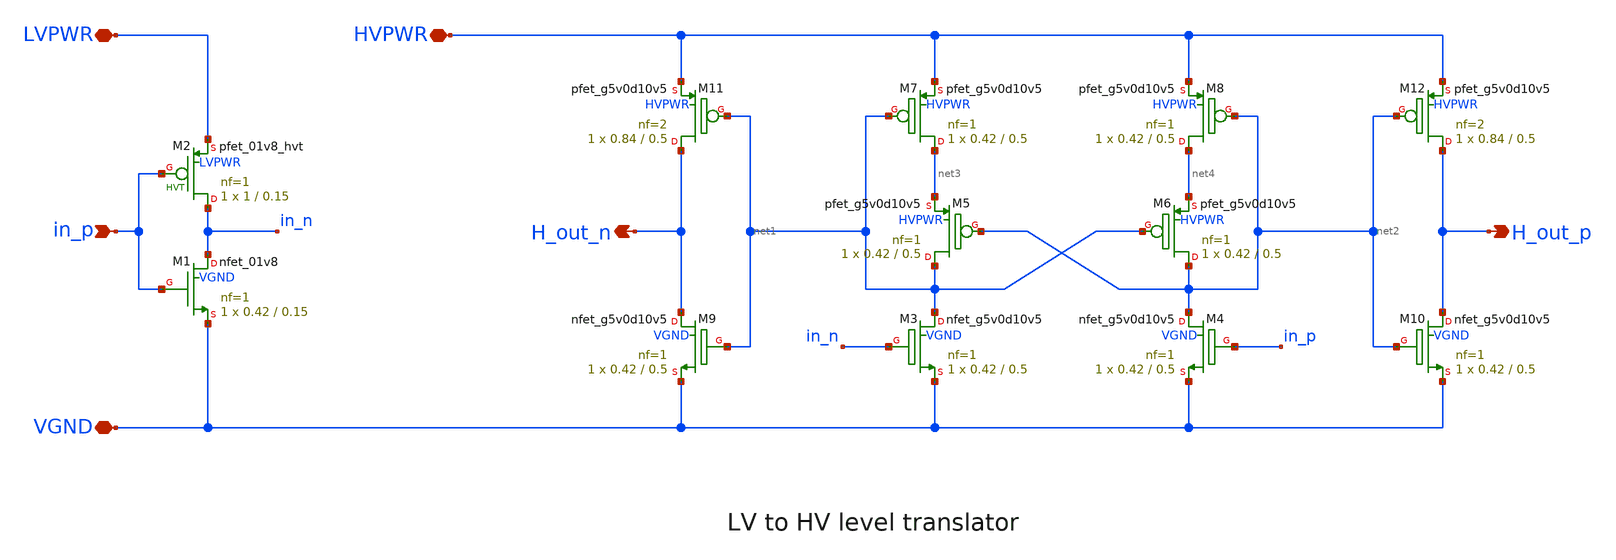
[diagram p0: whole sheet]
** sch_path: tt_um_analog_factory_test/xschem/lv2hv.sch
**.subckt lv2hv in_p VGND LVPWR HVPWR H_out_p H_out_n
*.ipin in_p
*.iopin VGND
*.iopin LVPWR
*.iopin HVPWR
*.opin H_out_p
*.opin H_out_n
XM12 H_out_p net2 HVPWR HVPWR sky130_fd_pr__pfet_g5v0d10v5 L=0.5 W=0.84 nf=2 ad='int((nf+1)/2) * W/nf * 0.29'
+ as='int((nf+2)/2) * W/nf * 0.29' pd='2*int((nf+1)/2) * (W/nf + 0.29)' ps='2*int((nf+2)/2) * (W/nf + 0.29)'
+ nrd='0.29 / W' nrs='0.29 / W' sa=0 sb=0 sd=0 mult=1 m=1
XM10 H_out_p net2 VGND VGND sky130_fd_pr__nfet_g5v0d10v5 L=0.5 W=0.42 nf=1 ad='int((nf+1)/2) * W/nf * 0.29'
+ as='int((nf+2)/2) * W/nf * 0.29' pd='2*int((nf+1)/2) * (W/nf + 0.29)' ps='2*int((nf+2)/2) * (W/nf + 0.29)'
+ nrd='0.29 / W' nrs='0.29 / W' sa=0 sb=0 sd=0 mult=1 m=1
XM11 H_out_n net1 HVPWR HVPWR sky130_fd_pr__pfet_g5v0d10v5 L=0.5 W=0.84 nf=2 ad='int((nf+1)/2) * W/nf * 0.29'
+ as='int((nf+2)/2) * W/nf * 0.29' pd='2*int((nf+1)/2) * (W/nf + 0.29)' ps='2*int((nf+2)/2) * (W/nf + 0.29)'
+ nrd='0.29 / W' nrs='0.29 / W' sa=0 sb=0 sd=0 mult=1 m=1
XM9 H_out_n net1 VGND VGND sky130_fd_pr__nfet_g5v0d10v5 L=0.5 W=0.42 nf=1 ad='int((nf+1)/2) * W/nf * 0.29'
+ as='int((nf+2)/2) * W/nf * 0.29' pd='2*int((nf+1)/2) * (W/nf + 0.29)' ps='2*int((nf+2)/2) * (W/nf + 0.29)'
+ nrd='0.29 / W' nrs='0.29 / W' sa=0 sb=0 sd=0 mult=1 m=1
XM1 in_n in_p VGND VGND sky130_fd_pr__nfet_01v8 L=0.15 W=0.42 nf=1 ad='int((nf+1)/2) * W/nf * 0.29' as='int((nf+2)/2) * W/nf * 0.29'
+ pd='2*int((nf+1)/2) * (W/nf + 0.29)' ps='2*int((nf+2)/2) * (W/nf + 0.29)' nrd='0.29 / W' nrs='0.29 / W'
+ sa=0 sb=0 sd=0 mult=1 m=1
XM2 in_n in_p LVPWR LVPWR sky130_fd_pr__pfet_01v8_hvt L=0.15 W=1 nf=1 ad='int((nf+1)/2) * W/nf * 0.29'
+ as='int((nf+2)/2) * W/nf * 0.29' pd='2*int((nf+1)/2) * (W/nf + 0.29)' ps='2*int((nf+2)/2) * (W/nf + 0.29)'
+ nrd='0.29 / W' nrs='0.29 / W' sa=0 sb=0 sd=0 mult=1 m=1
XM3 net1 in_n VGND VGND sky130_fd_pr__nfet_g5v0d10v5 L=0.5 W=0.42 nf=1 ad='int((nf+1)/2) * W/nf * 0.29'
+ as='int((nf+2)/2) * W/nf * 0.29' pd='2*int((nf+1)/2) * (W/nf + 0.29)' ps='2*int((nf+2)/2) * (W/nf + 0.29)'
+ nrd='0.29 / W' nrs='0.29 / W' sa=0 sb=0 sd=0 mult=1 m=1
XM4 net2 in_p VGND VGND sky130_fd_pr__nfet_g5v0d10v5 L=0.5 W=0.42 nf=1 ad='int((nf+1)/2) * W/nf * 0.29'
+ as='int((nf+2)/2) * W/nf * 0.29' pd='2*int((nf+1)/2) * (W/nf + 0.29)' ps='2*int((nf+2)/2) * (W/nf + 0.29)'
+ nrd='0.29 / W' nrs='0.29 / W' sa=0 sb=0 sd=0 mult=1 m=1
XM5 net1 net2 net3 HVPWR sky130_fd_pr__pfet_g5v0d10v5 L=0.5 W=0.42 nf=1 ad='int((nf+1)/2) * W/nf * 0.29'
+ as='int((nf+2)/2) * W/nf * 0.29' pd='2*int((nf+1)/2) * (W/nf + 0.29)' ps='2*int((nf+2)/2) * (W/nf + 0.29)'
+ nrd='0.29 / W' nrs='0.29 / W' sa=0 sb=0 sd=0 mult=1 m=1
XM6 net2 net1 net4 HVPWR sky130_fd_pr__pfet_g5v0d10v5 L=0.5 W=0.42 nf=1 ad='int((nf+1)/2) * W/nf * 0.29'
+ as='int((nf+2)/2) * W/nf * 0.29' pd='2*int((nf+1)/2) * (W/nf + 0.29)' ps='2*int((nf+2)/2) * (W/nf + 0.29)'
+ nrd='0.29 / W' nrs='0.29 / W' sa=0 sb=0 sd=0 mult=1 m=1
XM7 net3 net1 HVPWR HVPWR sky130_fd_pr__pfet_g5v0d10v5 L=0.5 W=0.42 nf=1 ad='int((nf+1)/2) * W/nf * 0.29'
+ as='int((nf+2)/2) * W/nf * 0.29' pd='2*int((nf+1)/2) * (W/nf + 0.29)' ps='2*int((nf+2)/2) * (W/nf + 0.29)'
+ nrd='0.29 / W' nrs='0.29 / W' sa=0 sb=0 sd=0 mult=1 m=1
XM8 net4 net2 HVPWR HVPWR sky130_fd_pr__pfet_g5v0d10v5 L=0.5 W=0.42 nf=1 ad='int((nf+1)/2) * W/nf * 0.29'
+ as='int((nf+2)/2) * W/nf * 0.29' pd='2*int((nf+1)/2) * (W/nf + 0.29)' ps='2*int((nf+2)/2) * (W/nf + 0.29)'
+ nrd='0.29 / W' nrs='0.29 / W' sa=0 sb=0 sd=0 mult=1 m=1
**.ends
.end
